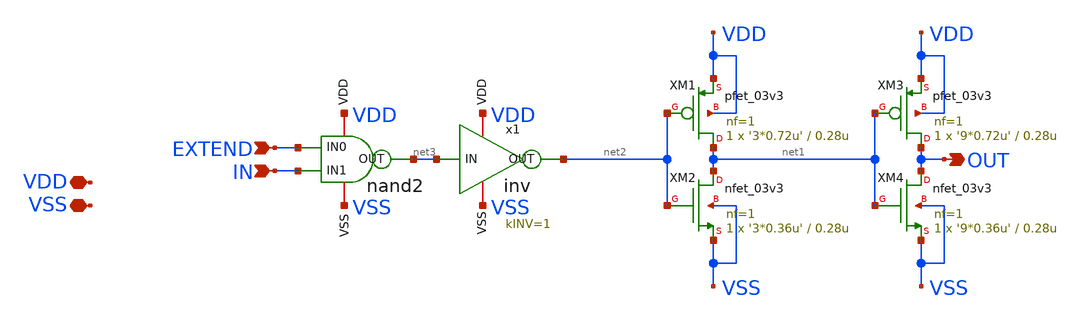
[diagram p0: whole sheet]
** sch_path: CAD7/sign_zero_extender.sch
**.subckt sign_zero_extender VDD VSS IN OUT EXTEND
*.iopin VDD
*.iopin VSS
*.ipin IN
*.opin OUT
*.ipin EXTEND
XM1 net1 net2 VDD VDD pfet_03v3 L=0.28u W='3*0.72u' nf=1 ad='int((nf+1)/2) * W/nf * 0.18u' as='int((nf+2)/2) * W/nf * 0.18u'
+ pd='2*int((nf+1)/2) * (W/nf + 0.18u)' ps='2*int((nf+2)/2) * (W/nf + 0.18u)' nrd='0.18u / W' nrs='0.18u / W'
+ sa=0 sb=0 sd=0 m=1
XM2 net1 net2 VSS VSS nfet_03v3 L=0.28u W='3*0.36u' nf=1 ad='int((nf+1)/2) * W/nf * 0.18u' as='int((nf+2)/2) * W/nf * 0.18u'
+ pd='2*int((nf+1)/2) * (W/nf + 0.18u)' ps='2*int((nf+2)/2) * (W/nf + 0.18u)' nrd='0.18u / W' nrs='0.18u / W'
+ sa=0 sb=0 sd=0 m=1
XM3 OUT net1 VDD VDD pfet_03v3 L=0.28u W='9*0.72u' nf=1 ad='int((nf+1)/2) * W/nf * 0.18u' as='int((nf+2)/2) * W/nf * 0.18u'
+ pd='2*int((nf+1)/2) * (W/nf + 0.18u)' ps='2*int((nf+2)/2) * (W/nf + 0.18u)' nrd='0.18u / W' nrs='0.18u / W'
+ sa=0 sb=0 sd=0 m=1
XM4 OUT net1 VSS VSS nfet_03v3 L=0.28u W='9*0.36u' nf=1 ad='int((nf+1)/2) * W/nf * 0.18u' as='int((nf+2)/2) * W/nf * 0.18u'
+ pd='2*int((nf+1)/2) * (W/nf + 0.18u)' ps='2*int((nf+2)/2) * (W/nf + 0.18u)' nrd='0.18u / W' nrs='0.18u / W'
+ sa=0 sb=0 sd=0 m=1
x1 VDD net3 net2 VSS inv kINV=1
**.ends
.end
